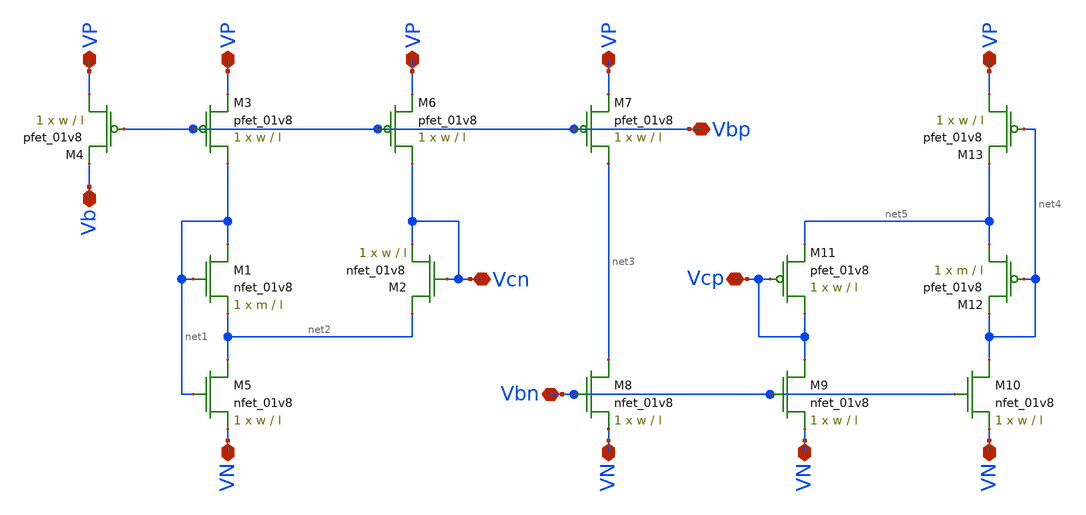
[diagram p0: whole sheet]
** sch_path: Mini_Project_3/bias_circ.sch
**.subckt bias_circ VP VN VP Vcn Vb VP VP Vbp Vbn VN VN Vcp VN VP
*.iopin VP
*.iopin VN
*.iopin VP
*.iopin Vcn
*.iopin Vb
*.iopin VP
*.iopin VP
*.iopin Vbp
*.iopin Vbn
*.iopin VN
*.iopin VN
*.iopin Vcp
*.iopin VN
*.iopin VP
XM3 net1 Vbp VP VDD sky130_fd_pr__pfet_01v8 L=l W=w nf=1 ad='int((nf+1)/2) * W/nf * 0.29' as='int((nf+2)/2) * W/nf * 0.29'
+ pd='2*int((nf+1)/2) * (W/nf + 0.29)' ps='2*int((nf+2)/2) * (W/nf + 0.29)' nrd='0.29 / W' nrs='0.29 / W'
+ sa=0 sb=0 sd=0 mult=1 m=1
XM4 VP Vbp Vb VDD sky130_fd_pr__pfet_01v8 L=l W=w nf=1 ad='int((nf+1)/2) * W/nf * 0.29' as='int((nf+2)/2) * W/nf * 0.29'
+ pd='2*int((nf+1)/2) * (W/nf + 0.29)' ps='2*int((nf+2)/2) * (W/nf + 0.29)' nrd='0.29 / W' nrs='0.29 / W'
+ sa=0 sb=0 sd=0 mult=1 m=1
XM6 Vcn Vbp VP VDD sky130_fd_pr__pfet_01v8 L=l W=w nf=1 ad='int((nf+1)/2) * W/nf * 0.29' as='int((nf+2)/2) * W/nf * 0.29'
+ pd='2*int((nf+1)/2) * (W/nf + 0.29)' ps='2*int((nf+2)/2) * (W/nf + 0.29)' nrd='0.29 / W' nrs='0.29 / W'
+ sa=0 sb=0 sd=0 mult=1 m=1
XM1 net1 net1 net2 GND sky130_fd_pr__nfet_01v8 L=l W=m nf=1 ad='int((nf+1)/2) * W/nf * 0.29' as='int((nf+2)/2) * W/nf * 0.29'
+ pd='2*int((nf+1)/2) * (W/nf + 0.29)' ps='2*int((nf+2)/2) * (W/nf + 0.29)' nrd='0.29 / W' nrs='0.29 / W'
+ sa=0 sb=0 sd=0 mult=1 m=1
XM2 net2 Vcn Vcn GND sky130_fd_pr__nfet_01v8 L=l W=w nf=1 ad='int((nf+1)/2) * W/nf * 0.29' as='int((nf+2)/2) * W/nf * 0.29'
+ pd='2*int((nf+1)/2) * (W/nf + 0.29)' ps='2*int((nf+2)/2) * (W/nf + 0.29)' nrd='0.29 / W' nrs='0.29 / W'
+ sa=0 sb=0 sd=0 mult=1 m=1
XM5 net2 net1 VN GND sky130_fd_pr__nfet_01v8 L=l W=w nf=1 ad='int((nf+1)/2) * W/nf * 0.29' as='int((nf+2)/2) * W/nf * 0.29'
+ pd='2*int((nf+1)/2) * (W/nf + 0.29)' ps='2*int((nf+2)/2) * (W/nf + 0.29)' nrd='0.29 / W' nrs='0.29 / W'
+ sa=0 sb=0 sd=0 mult=1 m=1
XM7 net3 Vbp VP VDD sky130_fd_pr__pfet_01v8 L=l W=w nf=1 ad='int((nf+1)/2) * W/nf * 0.29' as='int((nf+2)/2) * W/nf * 0.29'
+ pd='2*int((nf+1)/2) * (W/nf + 0.29)' ps='2*int((nf+2)/2) * (W/nf + 0.29)' nrd='0.29 / W' nrs='0.29 / W'
+ sa=0 sb=0 sd=0 mult=1 m=1
XM8 net3 Vbn VN GND sky130_fd_pr__nfet_01v8 L=l W=w nf=1 ad='int((nf+1)/2) * W/nf * 0.29' as='int((nf+2)/2) * W/nf * 0.29'
+ pd='2*int((nf+1)/2) * (W/nf + 0.29)' ps='2*int((nf+2)/2) * (W/nf + 0.29)' nrd='0.29 / W' nrs='0.29 / W'
+ sa=0 sb=0 sd=0 mult=1 m=1
XM9 Vcp Vbn VN GND sky130_fd_pr__nfet_01v8 L=l W=w nf=1 ad='int((nf+1)/2) * W/nf * 0.29' as='int((nf+2)/2) * W/nf * 0.29'
+ pd='2*int((nf+1)/2) * (W/nf + 0.29)' ps='2*int((nf+2)/2) * (W/nf + 0.29)' nrd='0.29 / W' nrs='0.29 / W'
+ sa=0 sb=0 sd=0 mult=1 m=1
XM10 net4 Vbn VN GND sky130_fd_pr__nfet_01v8 L=l W=w nf=1 ad='int((nf+1)/2) * W/nf * 0.29' as='int((nf+2)/2) * W/nf * 0.29'
+ pd='2*int((nf+1)/2) * (W/nf + 0.29)' ps='2*int((nf+2)/2) * (W/nf + 0.29)' nrd='0.29 / W' nrs='0.29 / W'
+ sa=0 sb=0 sd=0 mult=1 m=1
XM11 Vcp Vcp net5 VDD sky130_fd_pr__pfet_01v8 L=l W=w nf=1 ad='int((nf+1)/2) * W/nf * 0.29' as='int((nf+2)/2) * W/nf * 0.29'
+ pd='2*int((nf+1)/2) * (W/nf + 0.29)' ps='2*int((nf+2)/2) * (W/nf + 0.29)' nrd='0.29 / W' nrs='0.29 / W'
+ sa=0 sb=0 sd=0 mult=1 m=1
XM12 net5 net4 net4 VDD sky130_fd_pr__pfet_01v8 L=l W=m nf=1 ad='int((nf+1)/2) * W/nf * 0.29' as='int((nf+2)/2) * W/nf * 0.29'
+ pd='2*int((nf+1)/2) * (W/nf + 0.29)' ps='2*int((nf+2)/2) * (W/nf + 0.29)' nrd='0.29 / W' nrs='0.29 / W'
+ sa=0 sb=0 sd=0 mult=1 m=1
XM13 VP net4 net5 VDD sky130_fd_pr__pfet_01v8 L=l W=w nf=1 ad='int((nf+1)/2) * W/nf * 0.29' as='int((nf+2)/2) * W/nf * 0.29'
+ pd='2*int((nf+1)/2) * (W/nf + 0.29)' ps='2*int((nf+2)/2) * (W/nf + 0.29)' nrd='0.29 / W' nrs='0.29 / W'
+ sa=0 sb=0 sd=0 mult=1 m=1
**.ends
.end
